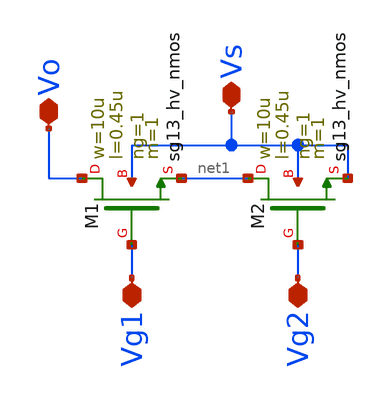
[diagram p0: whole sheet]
** sch_path: schematics/DCDCBuck_vto1p1_derecho.sch
**.subckt DCDCBuck_vto1p1_derecho Vs Vg1 Vg2 Vo
*.iopin Vs
*.iopin Vg1
*.iopin Vg2
*.iopin Vo
MM2 net1 Vg2 Vs Vs sg13_hv_nmos w=10u l=0.45u ng=1 m=1 mm_ok=1
MM1 Vo Vg1 net1 Vs sg13_hv_nmos w=10u l=0.45u ng=1 m=1 mm_ok=1
**.ends
.end
